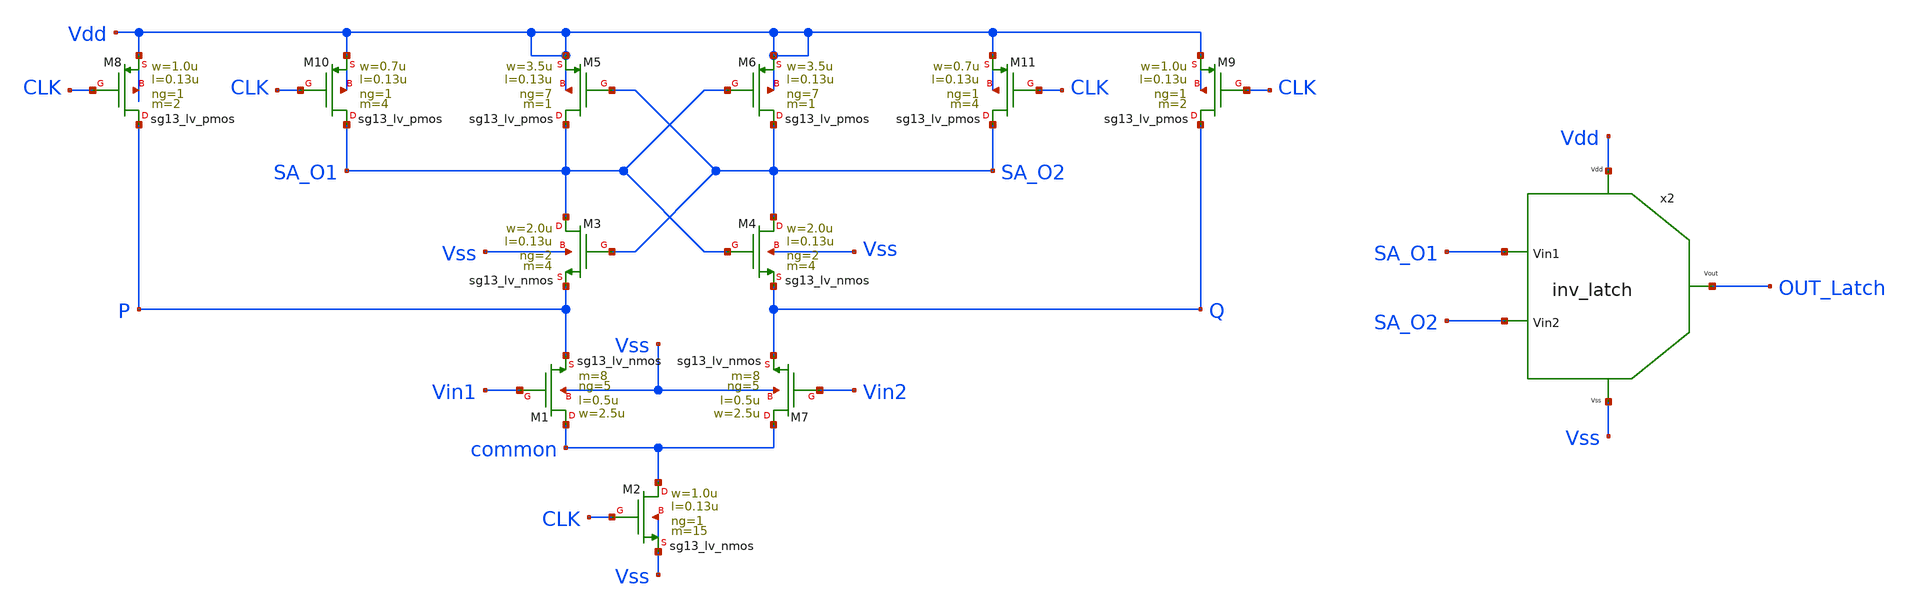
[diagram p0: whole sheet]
** sch_path: klayout/LVS/SA_LATCH.sch
**.subckt SA_LATCH
XM4 SA_O2 SA_O1 Q Vss sg13_lv_nmos w=2.0u l=0.13u ng=2 m=4 mm_ok=1
XM6 SA_O2 SA_O1 Vdd Vdd sg13_lv_pmos w=3.5u l=0.13u ng=7 m=1 mm_ok=1
XM11 SA_O2 CLK Vdd Vdd sg13_lv_pmos w=0.7u l=0.13u ng=1 m=4 mm_ok=1
XM9 Q CLK Vdd Vdd sg13_lv_pmos w=1.0u l=0.13u ng=1 m=2 mm_ok=1
XM3 SA_O1 SA_O2 P Vss sg13_lv_nmos w=2.0u l=0.13u ng=2 m=4 mm_ok=1
XM5 SA_O1 SA_O2 Vdd Vdd sg13_lv_pmos w=3.5u l=0.13u ng=7 m=1 mm_ok=1
XM10 SA_O1 CLK Vdd Vdd sg13_lv_pmos w=0.7u l=0.13u ng=1 m=4 mm_ok=1
XM8 P CLK Vdd Vdd sg13_lv_pmos w=1.0u l=0.13u ng=1 m=2 mm_ok=1
XM1 common Vin1 P Vss sg13_lv_nmos w=2.5u l=0.5u ng=5 m=8 mm_ok=1
XM2 common CLK Vss Vss sg13_lv_nmos w=1.0u l=0.13u ng=1 m=15 mm_ok=1
XM7 common Vin2 Q Vss sg13_lv_nmos w=2.5u l=0.5u ng=5 m=8 mm_ok=1
x2 Vdd OUT_Latch Vss SA_O1 SA_O2 inv_latch
**.ends

* expanding   symbol:
*+  /workspaces/usm-vlsi-tools/shared_xserver/proyecto-IPD413/xschem/sch/inv_latch.sym # of pins=5
** sym_path: xschem/sch/inv_latch.sym
** sch_path: xschem/sch/inv_latch.sch
.subckt inv_latch Vdd Vout Vss Vin1 Vin2
*.opin Vout
*.ipin Vdd
*.ipin Vdd
*.ipin Vin1
*.ipin Vss
*.ipin Vss
*.ipin Vdd
*.ipin Vss
*.ipin Vdd
*.ipin Vin2
*.ipin Vss
*.ipin Vss
x1 net1 Vout Vdd Vss inv_lv
x2 Vout net1 Vdd Vss inv_lv
XM1 net1 net2 Vss Vss sg13_lv_nmos w=1.5u l=0.13u ng=1 m=1 mm_ok=1
x3 Vin1 net2 Vdd Vss inv_lv
XM2 Vout net3 Vss Vss sg13_lv_nmos w=1.5u l=0.13u ng=1 m=1 mm_ok=1
x4 Vin2 net3 Vdd Vss inv_lv
.ends


* expanding   symbol:  proyecto-IPD413/xschem/sch/inv_lv.sym # of pins=4
** sym_path: xschem/sch/inv_lv.sym
** sch_path: xschem/sch/inv_lv.sch
.subckt inv_lv Vin Vout Vdd Vss
*.ipin Vdd
*.ipin Vss
*.ipin Vin
*.opin Vout
XM1 Vss Vin Vout Vss sg13_lv_nmos w=1u l=0.13u ng=1 m=1 mm_ok=1
XM2 Vout Vin Vdd Vdd sg13_lv_pmos w=2.3u l=0.13u ng=1 m=1 mm_ok=1
.ends

.end
